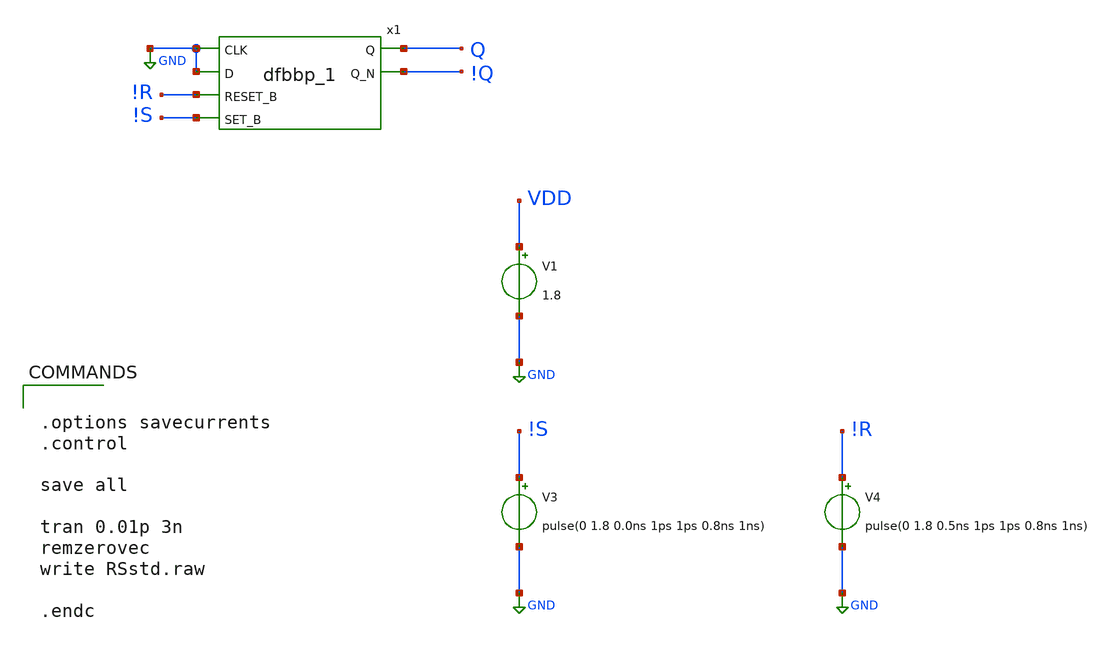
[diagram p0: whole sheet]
** sch_path: RSlatch/xschem/RSstd.sch
.lib $::SKYWATER_MODELS/sky130.lib.spice tt
.include $::SKYWATER_STDCELLS/sky130_fd_sc_hd.spice

**.subckt RSstd
V1 VDD GND 1.8
V4 !R GND pulse(0 1.8 0.5ns 1ps 1ps 0.8ns 1ns)
V3 !S GND pulse(0 1.8 0.0ns 1ps 1ps 0.8ns 1ns)
x1 GND GND !R !S GND GND VDD VDD Q !Q sky130_fd_sc_hd__dfbbp_1
**** begin user architecture code


.options savecurrents
.control

save all

tran 0.01p 3n
remzerovec
write RSstd.raw

.endc


**** end user architecture code
**.ends
.GLOBAL GND
.end
